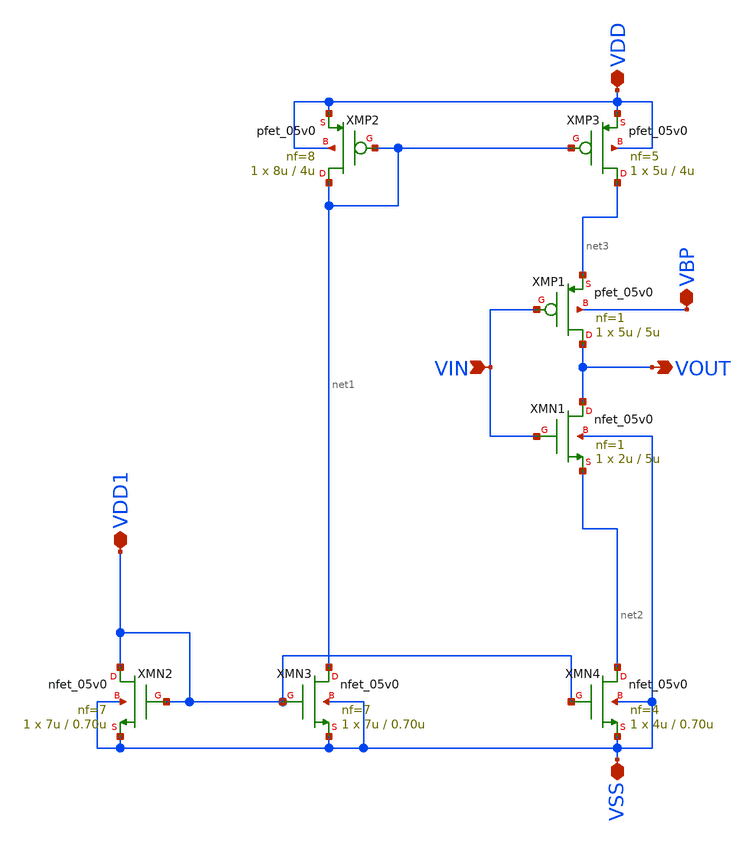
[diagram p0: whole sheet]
** sch_path: xschem/vco/vco_inv-n-pmosmirr_forlvs.sch
**.subckt vco_inv-n-pmosmirr_forlvs VSS VDD1 VIN VOUT VBP VDD
*.iopin VSS
*.iopin VDD1
*.ipin VIN
*.opin VOUT
*.iopin VBP
*.iopin VDD
XMN2 VDD1 VDD1 VSS VSS nfet_05v0 L=0.70u W=7u nf=7 ad='int((nf+1)/2) * W/nf * 0.18u' as='int((nf+2)/2) * W/nf * 0.18u'
+ pd='2*int((nf+1)/2) * (W/nf + 0.18u)' ps='2*int((nf+2)/2) * (W/nf + 0.18u)' nrd='0.18u / W' nrs='0.18u / W'
+ sa=0 sb=0 sd=0 m=1
XMN3 net1 VDD1 VSS VSS nfet_05v0 L=0.70u W=7u nf=7 ad='int((nf+1)/2) * W/nf * 0.18u' as='int((nf+2)/2) * W/nf * 0.18u'
+ pd='2*int((nf+1)/2) * (W/nf + 0.18u)' ps='2*int((nf+2)/2) * (W/nf + 0.18u)' nrd='0.18u / W' nrs='0.18u / W'
+ sa=0 sb=0 sd=0 m=1
XMN4 net2 VDD1 VSS VSS nfet_05v0 L=0.70u W=4u nf=4 ad='int((nf+1)/2) * W/nf * 0.18u' as='int((nf+2)/2) * W/nf * 0.18u'
+ pd='2*int((nf+1)/2) * (W/nf + 0.18u)' ps='2*int((nf+2)/2) * (W/nf + 0.18u)' nrd='0.18u / W' nrs='0.18u / W'
+ sa=0 sb=0 sd=0 m=1
XMN1 VOUT VIN net2 VSS nfet_05v0 L=5u W=2u nf=1 ad='int((nf+1)/2) * W/nf * 0.18u' as='int((nf+2)/2) * W/nf * 0.18u'
+ pd='2*int((nf+1)/2) * (W/nf + 0.18u)' ps='2*int((nf+2)/2) * (W/nf + 0.18u)' nrd='0.18u / W' nrs='0.18u / W'
+ sa=0 sb=0 sd=0 m=1
XMP1 VOUT VIN net3 VBP pfet_05v0 L=5u W=5u nf=1 ad='int((nf+1)/2) * W/nf * 0.18u' as='int((nf+2)/2) * W/nf * 0.18u'
+ pd='2*int((nf+1)/2) * (W/nf + 0.18u)' ps='2*int((nf+2)/2) * (W/nf + 0.18u)' nrd='0.18u / W' nrs='0.18u / W'
+ sa=0 sb=0 sd=0 m=1
XMP2 net1 net1 VDD VDD pfet_05v0 L=4u W=8u nf=8 ad='int((nf+1)/2) * W/nf * 0.18u' as='int((nf+2)/2) * W/nf * 0.18u'
+ pd='2*int((nf+1)/2) * (W/nf + 0.18u)' ps='2*int((nf+2)/2) * (W/nf + 0.18u)' nrd='0.18u / W' nrs='0.18u / W'
+ sa=0 sb=0 sd=0 m=1
XMP3 net3 net1 VDD VDD pfet_05v0 L=4u W=5u nf=5 ad='int((nf+1)/2) * W/nf * 0.18u' as='int((nf+2)/2) * W/nf * 0.18u'
+ pd='2*int((nf+1)/2) * (W/nf + 0.18u)' ps='2*int((nf+2)/2) * (W/nf + 0.18u)' nrd='0.18u / W' nrs='0.18u / W'
+ sa=0 sb=0 sd=0 m=1
**.ends
.end
